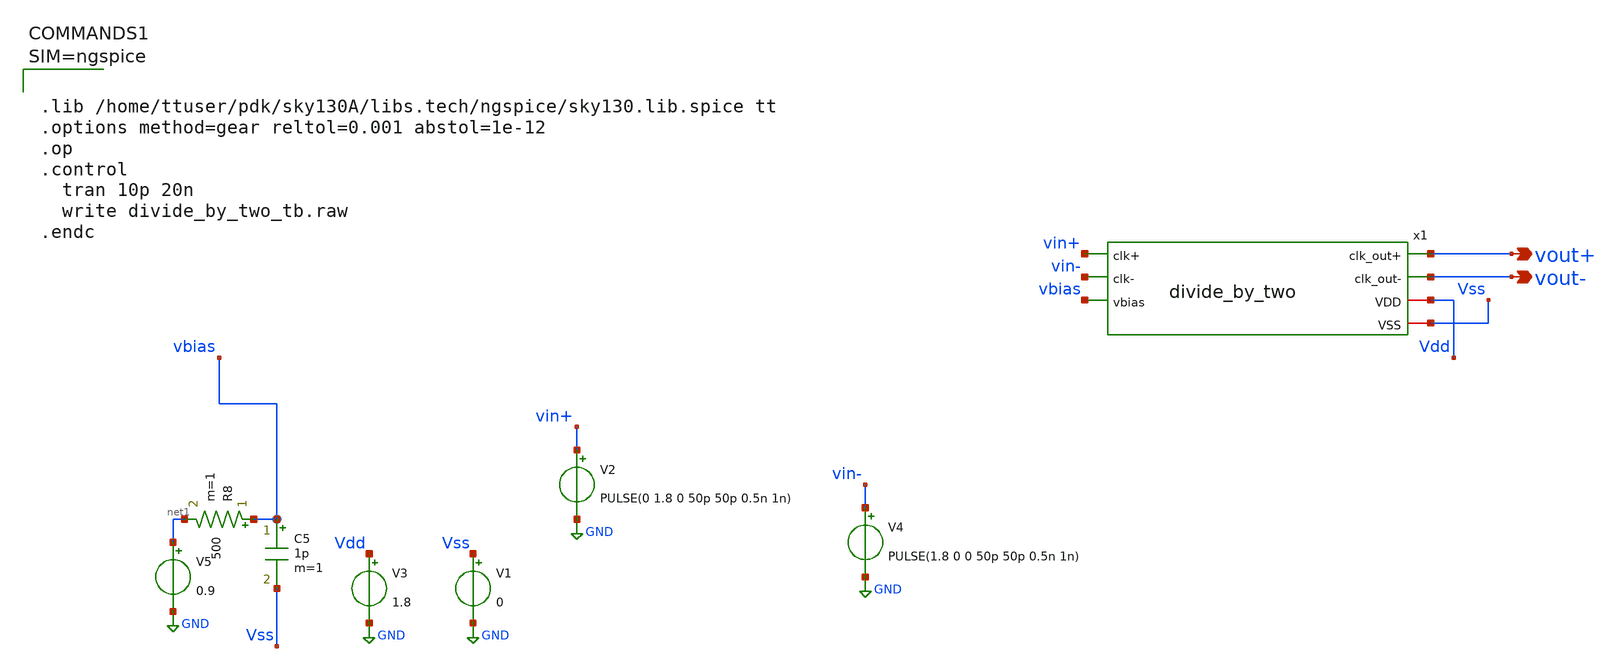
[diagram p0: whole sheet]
** sch_path: xschem/attic/divide_by_two_tb.sch
**.subckt divide_by_two_tb vout+ vout-
*.opin vout+
*.opin vout-
V3 Vdd GND 1.8
V1 Vss GND 0
V2 vin+ GND PULSE(0 1.8 0 50p 50p 0.5n 1n)
V4 vin- GND PULSE(1.8 0 0 50p 50p 0.5n 1n)
V5 net1 GND 0.9
R8 vbias net1 500 m=1
C5 vbias Vss 1p m=1
x1 vout+ vout- vin+ vin- vbias Vdd Vss divide_by_two
**** begin user architecture code



.lib /home/ttuser/pdk/sky130A/libs.tech/ngspice/sky130.lib.spice tt
.options method=gear reltol=0.001 abstol=1e-12
.op
.control
  tran 10p 20n
  write divide_by_two_tb.raw
.endc



**** end user architecture code
**.ends
.GLOBAL GND
.end
